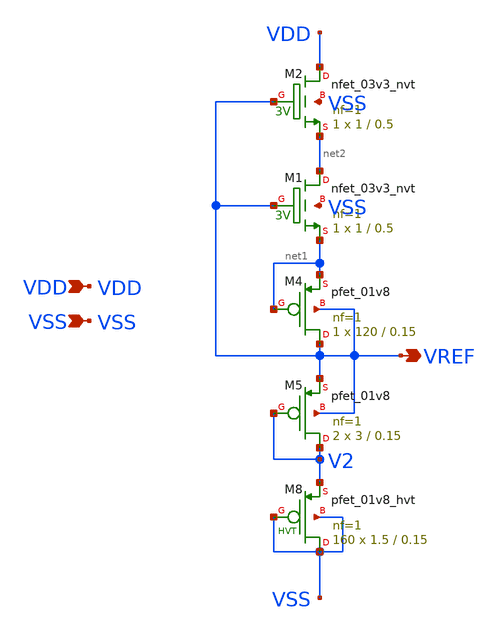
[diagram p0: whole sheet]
** sch_path: design/LELO_SVOD_SKY130A/LELO_SVOD_VTREF.sch
**.subckt LELO_SVOD_VTREF VDD VSS VREF
*.ipin VDD
*.ipin VSS
*.opin VREF
XM4 VREF net1 net1 VREF sky130_fd_pr__pfet_01v8 L=0.15 W=120 nf=1 ad='int((1 + 1)/2) * 120 / 1 * 0.29'
+ as='int((1 + 2)/2) * 120 / 1 * 0.29' pd='2*int((1 + 1)/2) * (120 / 1 + 0.29)' ps='2*int((1 + 2)/2) * (120 / 1 + 0.29)'
+ nrd='0.29 / 120 ' nrs='0.29 / 120 ' sa=0 sb=0 sd=0 mult=1 m=1
XM5 V2 V2 VREF VREF sky130_fd_pr__pfet_01v8 L=0.15 W=3 nf=1 ad='int((1 + 1)/2) * 3 / 1 * 0.29' as='int((1 + 2)/2) * 3 / 1 * 0.29'
+ pd='2*int((1 + 1)/2) * (3 / 1 + 0.29)' ps='2*int((1 + 2)/2) * (3 / 1 + 0.29)' nrd='0.29 / 3 ' nrs='0.29 / 3 '
+ sa=0 sb=0 sd=0 mult=2 m=2
XM8 VSS VSS V2 VSS sky130_fd_pr__pfet_01v8_hvt L=0.15 W=1.5 nf=1 ad='int((1 + 1)/2) * 1.5 / 1 * 0.29'
+ as='int((1 + 2)/2) * 1.5 / 1 * 0.29' pd='2*int((1 + 1)/2) * (1.5 / 1 + 0.29)' ps='2*int((1 + 2)/2) * (1.5 / 1 + 0.29)'
+ nrd='0.29 / 1.5 ' nrs='0.29 / 1.5 ' sa=0 sb=0 sd=0 mult=160 m=160
XM1 net2 VREF net1 VSS sky130_fd_pr__nfet_03v3_nvt L=0.5 W=1 nf=1 ad='int((1 + 1)/2) * 1 / 1 * 0.29'
+ as='int((1 + 2)/2) * 1 / 1 * 0.29' pd='2*int((1 + 1)/2) * (1 / 1 + 0.29)' ps='2*int((1 + 2)/2) * (1 / 1 + 0.29)'
+ nrd='0.29 / 1 ' nrs='0.29 / 1 ' sa=0 sb=0 sd=0 mult=1 m=1
XM2 VDD VREF net2 VSS sky130_fd_pr__nfet_03v3_nvt L=0.5 W=1 nf=1 ad='int((1 + 1)/2) * 1 / 1 * 0.29' as='int((1 + 2)/2) * 1 / 1 * 0.29'
+ pd='2*int((1 + 1)/2) * (1 / 1 + 0.29)' ps='2*int((1 + 2)/2) * (1 / 1 + 0.29)' nrd='0.29 / 1 ' nrs='0.29 / 1 '
+ sa=0 sb=0 sd=0 mult=1 m=1
**.ends
.end
